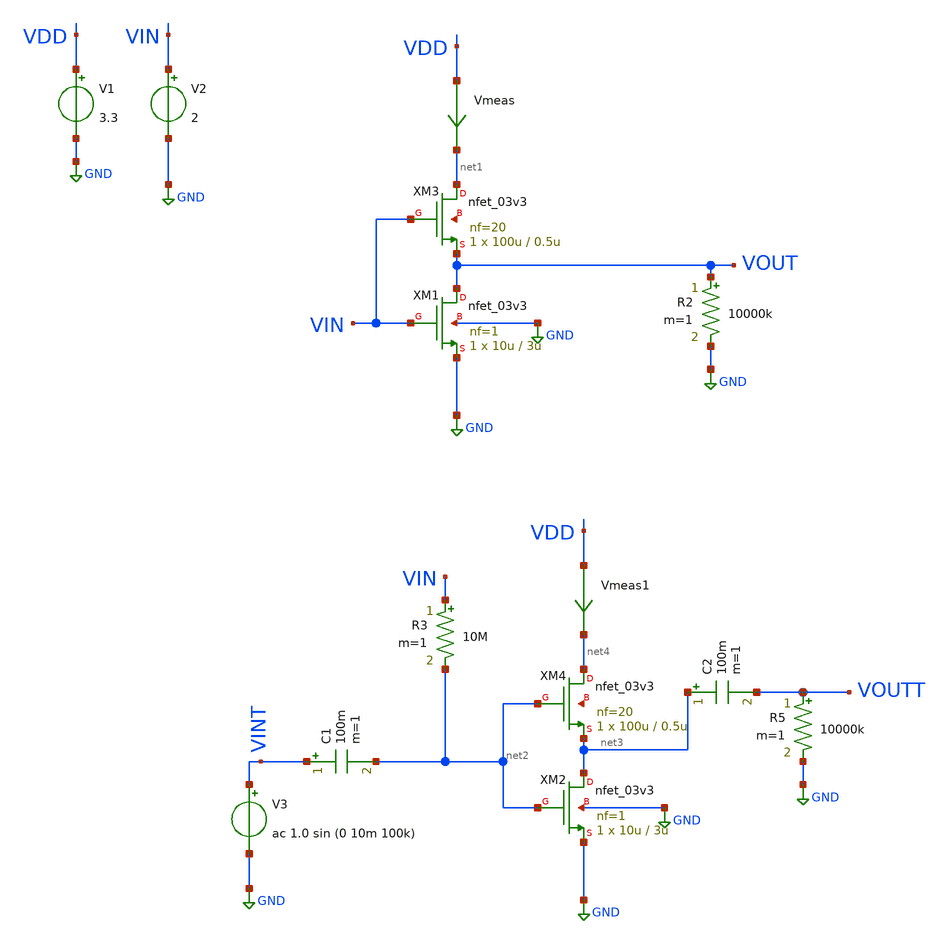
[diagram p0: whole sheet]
** sch_path: gain_with_load/simple_amp_with_load3.sch
**.subckt simple_amp_with_load3
XM1 VOUT VIN GND GND nfet_03v3 L=3u W=10u nf=1 ad='int((nf+1)/2) * W/nf * 0.18u' as='int((nf+2)/2) * W/nf * 0.18u'
+ pd='2*int((nf+1)/2) * (W/nf + 0.18u)' ps='2*int((nf+2)/2) * (W/nf + 0.18u)' nrd='0.18u / W' nrs='0.18u / W'
+ sa=0 sb=0 sd=0 m=1
Vmeas VDD net1 0
.save i(vmeas)
V1 VDD GND 3.3
V2 VIN GND 2
V3 VINT GND ac 1.0 sin (0 10m 100k)
R2 VOUT GND 10000k m=1
C1 VINT net2 100m m=1
R3 VIN net2 10M m=1
C2 net3 VOUTT 100m m=1
R5 VOUTT GND 10000k m=1
XM3 net1 VIN VOUT net5 nfet_03v3 L=0.5u W=100u nf=20 ad='int((nf+1)/2) * W/nf * 0.18u' as='int((nf+2)/2) * W/nf * 0.18u'
+ pd='2*int((nf+1)/2) * (W/nf + 0.18u)' ps='2*int((nf+2)/2) * (W/nf + 0.18u)' nrd='0.18u / W' nrs='0.18u / W'
+ sa=0 sb=0 sd=0 m=1
XM2 net3 net2 GND GND nfet_03v3 L=3u W=10u nf=1 ad='int((nf+1)/2) * W/nf * 0.18u' as='int((nf+2)/2) * W/nf * 0.18u'
+ pd='2*int((nf+1)/2) * (W/nf + 0.18u)' ps='2*int((nf+2)/2) * (W/nf + 0.18u)' nrd='0.18u / W' nrs='0.18u / W'
+ sa=0 sb=0 sd=0 m=1
Vmeas1 VDD net4 0
.save i(vmeas1)
XM4 net4 net2 net3 net6 nfet_03v3 L=0.5u W=100u nf=20 ad='int((nf+1)/2) * W/nf * 0.18u' as='int((nf+2)/2) * W/nf * 0.18u'
+ pd='2*int((nf+1)/2) * (W/nf + 0.18u)' ps='2*int((nf+2)/2) * (W/nf + 0.18u)' nrd='0.18u / W' nrs='0.18u / W'
+ sa=0 sb=0 sd=0 m=1
**** begin user architecture code



.include $::180MCU_MODELS/design.ngspice
*.lib $::180MCU_MODELS/sm141064.ngspice statistical
*.lib $::180MCU_MODELS/sm141064.ngspice res_statistical
.lib $::180MCU_MODELS/sm141064.ngspice typical
.lib $::180MCU_MODELS/sm141064.ngspice res_typical
.lib $::180MCU_MODELS/sm141064.ngspice moscap_typical
.lib $::180MCU_MODELS/sm141064.ngspice bjt_typical
.lib $::180MCU_MODELS/sm141064.ngspice diode_typical
.lib $::180MCU_MODELS/sm141064.ngspice mimcap_typical
.TEMP 27

.param   sw_stat_global = 1   sw_stat_mism = 1  mc_skew = 3  res_mc_skew = 3  cap_mc_skew = 3
+  fnoicor = 1









.control
save all
dc V2 0 3.3 0.01
plot v(VOUT) v(VIN) deriv(v(VOUT))
plot i(Vmeas)
plot deriv(v(VOUT))
tran 10ns 20u
plot (v(VINT)) (v(VOUTT))
fft v(VOUTT) v(VINT)
plot mag(v(VOUTT)) mag(v(VINT))


ac dec 20 1 50G
plot v(VOUTT)
.endc

**** end user architecture code
**.ends
.GLOBAL GND
.end
